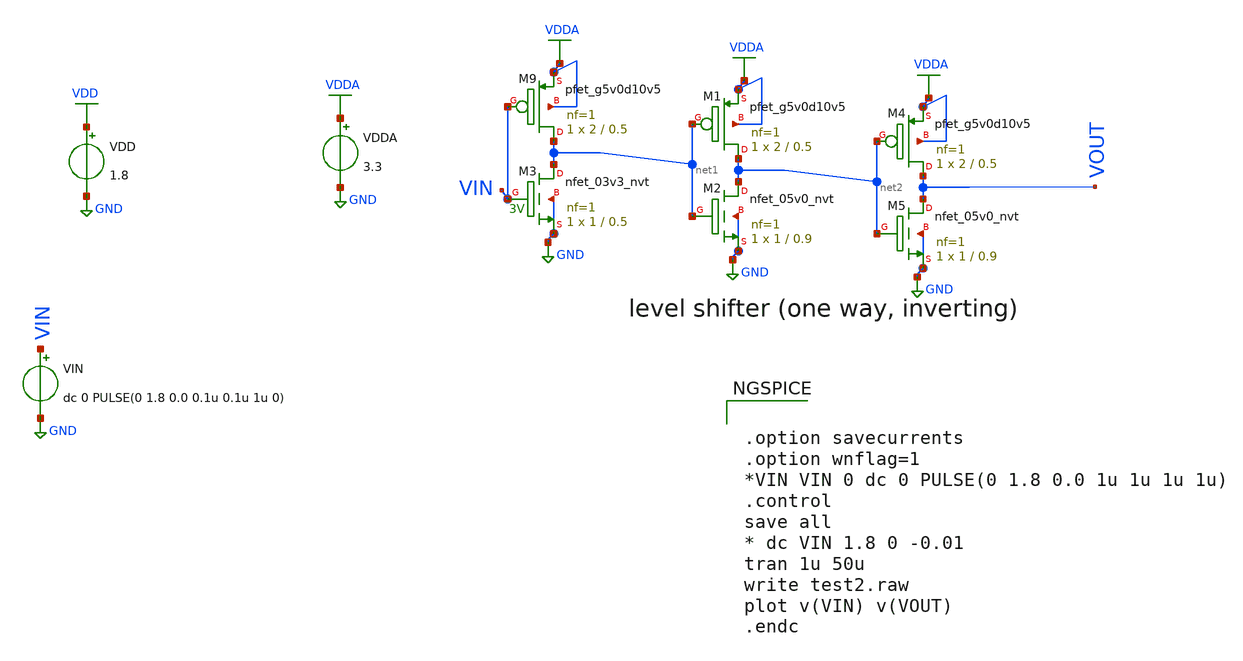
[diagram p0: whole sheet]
** sch_path: xschem/lthinverter.sch
**.subckt lthinverter
VDD VDD GND 1.8
VIN VIN GND dc 0 PULSE(0 1.8 0.0 0.1u 0.1u 1u 0)
VDDA VDDA GND 3.3
XM9 net1 VIN VDDA VDDA sky130_fd_pr__pfet_g5v0d10v5 L=0.5 W=2 nf=1 ad='int((1 + 1)/2) * 2 / 1 * 0.29'
+ as='int((1 + 2)/2) * 2 / 1 * 0.29' pd='2*int((1 + 1)/2) * (2 / 1 + 0.29)' ps='2*int((1 + 2)/2) * (2 / 1 + 0.29)'
+ nrd='0.29 / 2 ' nrs='0.29 / 2 ' sa=0 sb=0 sd=0 mult=1 m=1
XM1 net2 net1 VDDA VDDA sky130_fd_pr__pfet_g5v0d10v5 L=0.5 W=2 nf=1 ad='int((1 + 1)/2) * 2 / 1 * 0.29'
+ as='int((1 + 2)/2) * 2 / 1 * 0.29' pd='2*int((1 + 1)/2) * (2 / 1 + 0.29)' ps='2*int((1 + 2)/2) * (2 / 1 + 0.29)'
+ nrd='0.29 / 2 ' nrs='0.29 / 2 ' sa=0 sb=0 sd=0 mult=1 m=1
XM2 net2 net1 GND GND sky130_fd_pr__nfet_05v0_nvt L=0.9 W=1 nf=1 ad='int((1 + 1)/2) * 1 / 1 * 0.29' as='int((1 + 2)/2) * 1 / 1 * 0.29'
+ pd='2*int((1 + 1)/2) * (1 / 1 + 0.29)' ps='2*int((1 + 2)/2) * (1 / 1 + 0.29)' nrd='0.29 / 1 ' nrs='0.29 / 1 '
+ sa=0 sb=0 sd=0 mult=1 m=1
XM3 net1 VIN GND GND sky130_fd_pr__nfet_03v3_nvt L=0.5 W=1 nf=1 ad='int((1 + 1)/2) * 1 / 1 * 0.29' as='int((1 + 2)/2) * 1 / 1 * 0.29'
+ pd='2*int((1 + 1)/2) * (1 / 1 + 0.29)' ps='2*int((1 + 2)/2) * (1 / 1 + 0.29)' nrd='0.29 / 1 ' nrs='0.29 / 1 '
+ sa=0 sb=0 sd=0 mult=1 m=1
XM4 VOUT net2 VDDA VDDA sky130_fd_pr__pfet_g5v0d10v5 L=0.5 W=2 nf=1 ad='int((1 + 1)/2) * 2 / 1 * 0.29'
+ as='int((1 + 2)/2) * 2 / 1 * 0.29' pd='2*int((1 + 1)/2) * (2 / 1 + 0.29)' ps='2*int((1 + 2)/2) * (2 / 1 + 0.29)'
+ nrd='0.29 / 2 ' nrs='0.29 / 2 ' sa=0 sb=0 sd=0 mult=1 m=1
XM5 VOUT net2 GND GND sky130_fd_pr__nfet_05v0_nvt L=0.9 W=1 nf=1 ad='int((1 + 1)/2) * 1 / 1 * 0.29' as='int((1 + 2)/2) * 1 / 1 * 0.29'
+ pd='2*int((1 + 1)/2) * (1 / 1 + 0.29)' ps='2*int((1 + 2)/2) * (1 / 1 + 0.29)' nrd='0.29 / 1 ' nrs='0.29 / 1 '
+ sa=0 sb=0 sd=0 mult=1 m=1
**** begin user architecture code

** opencircuitdesign pdks install
.lib $::SKYWATER_MODELS/sky130.lib.spice tt




.option savecurrents
.option wnflag=1
*VIN VIN 0 dc 0 PULSE(0 1.8 0.0 1u 1u 1u 1u)
.control
save all
* dc VIN 1.8 0 -0.01
tran 1u 50u
write test2.raw
plot v(VIN) v(VOUT)
.endc


**** end user architecture code
**.ends
.GLOBAL GND
.GLOBAL VDD
.GLOBAL VDDA
.end
